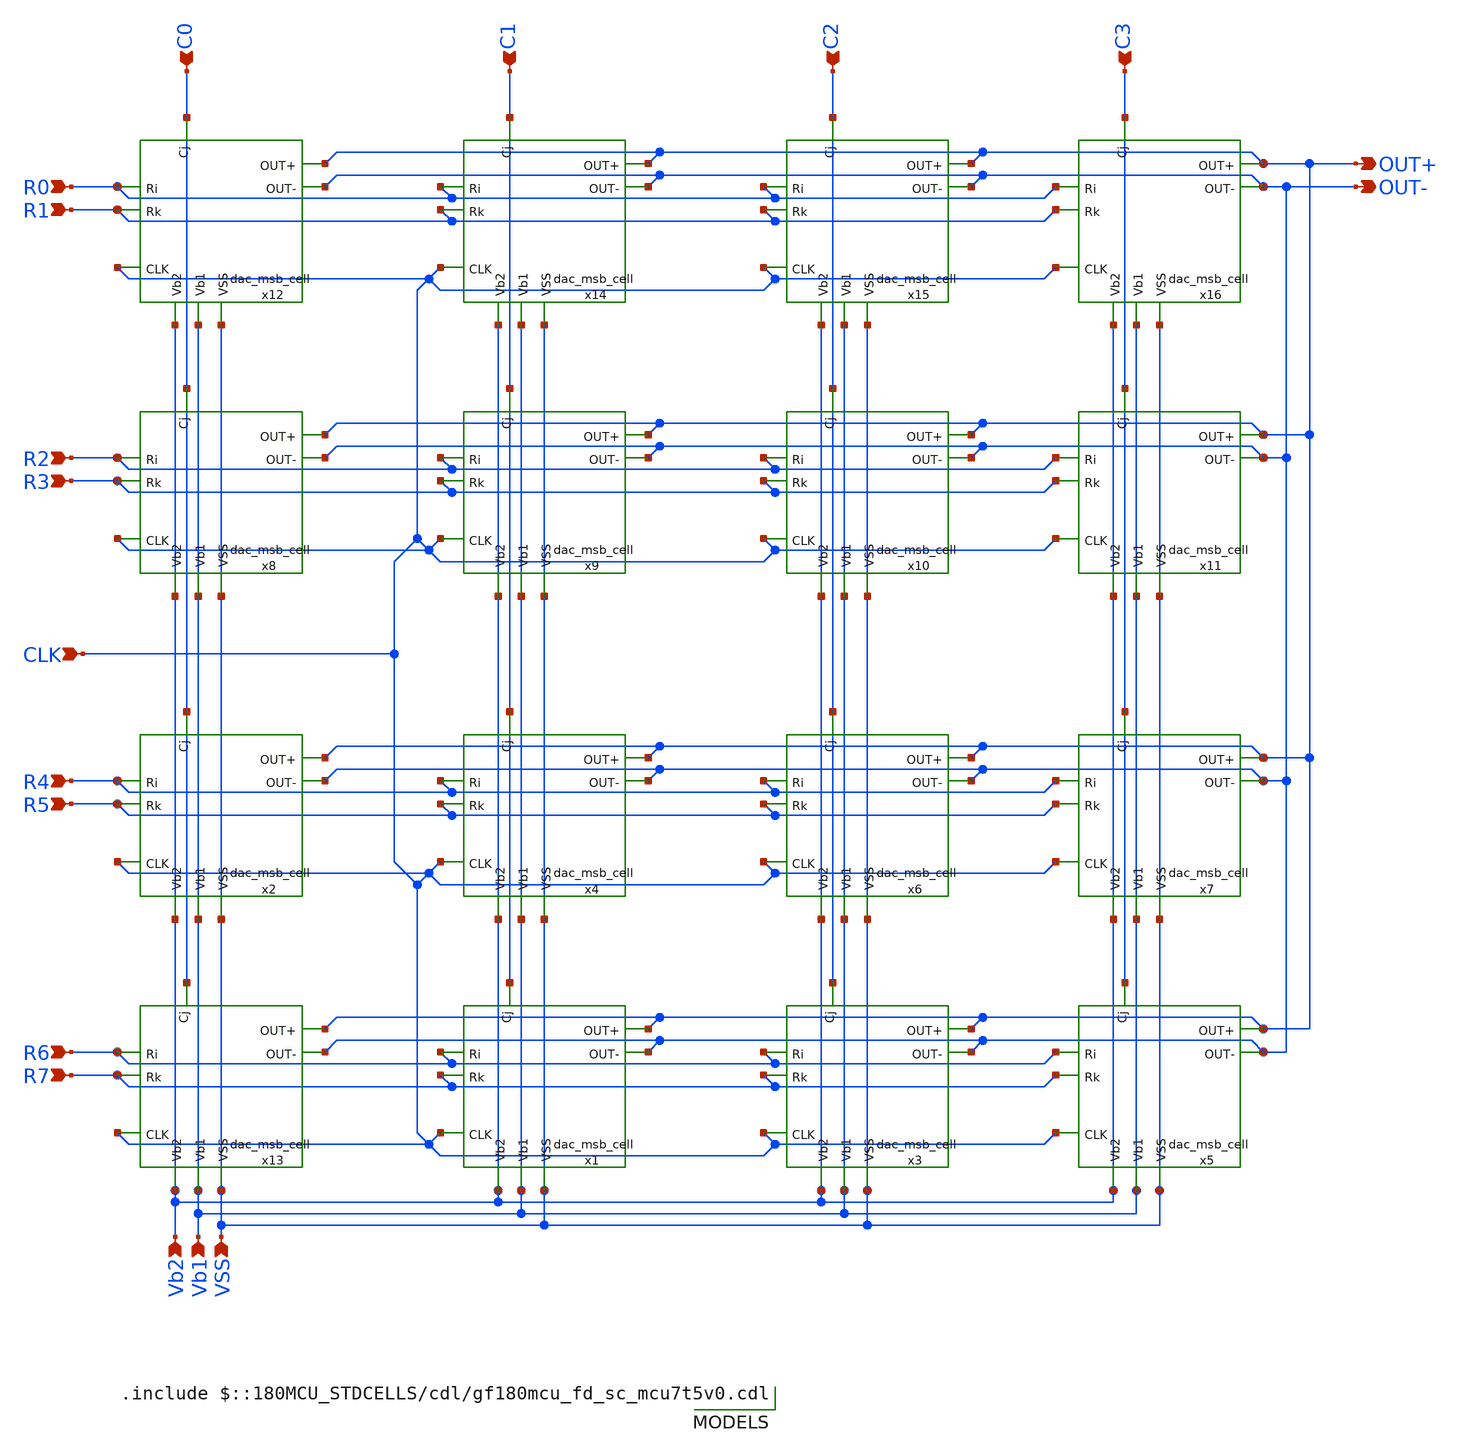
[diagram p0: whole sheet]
** sch_path: DAC/xschem/dac_msb_quarter_matrix.sch
**.subckt dac_msb_quarter_matrix CLK R0 R1 R2 R3 R4 R5 R6 R7 C0 C1 C2 C3 VSS Vb2 Vb1 OUT+ OUT-
*.ipin CLK
*.ipin R0
*.ipin R1
*.ipin R2
*.ipin R3
*.ipin R4
*.ipin R5
*.ipin R6
*.ipin R7
*.ipin C0
*.ipin C1
*.ipin C2
*.ipin C3
*.ipin VSS
*.ipin Vb2
*.ipin Vb1
*.opin OUT+
*.opin OUT-
x13 C0 R6 R7 CLK Vb2 Vb1 VSS OUT+ OUT- DVDD DVSS dac_msb_cell
x1 C1 R6 R7 CLK Vb2 Vb1 VSS OUT+ OUT- DVDD DVSS dac_msb_cell
x3 C2 R6 R7 CLK Vb2 Vb1 VSS OUT+ OUT- DVDD DVSS dac_msb_cell
x5 C3 R6 R7 CLK Vb2 Vb1 VSS OUT+ OUT- DVDD DVSS dac_msb_cell
x2 C0 R4 R5 CLK Vb2 Vb1 VSS OUT+ OUT- DVDD DVSS dac_msb_cell
x4 C1 R4 R5 CLK Vb2 Vb1 VSS OUT+ OUT- DVDD DVSS dac_msb_cell
x6 C2 R4 R5 CLK Vb2 Vb1 VSS OUT+ OUT- DVDD DVSS dac_msb_cell
x7 C3 R4 R5 CLK Vb2 Vb1 VSS OUT+ OUT- DVDD DVSS dac_msb_cell
x8 C0 R2 R3 CLK Vb2 Vb1 VSS OUT+ OUT- DVDD DVSS dac_msb_cell
x9 C1 R2 R3 CLK Vb2 Vb1 VSS OUT+ OUT- DVDD DVSS dac_msb_cell
x10 C2 R2 R3 CLK Vb2 Vb1 VSS OUT+ OUT- DVDD DVSS dac_msb_cell
x11 C3 R2 R3 CLK Vb2 Vb1 VSS OUT+ OUT- DVDD DVSS dac_msb_cell
x12 C0 R0 R1 CLK Vb2 Vb1 VSS OUT+ OUT- DVDD DVSS dac_msb_cell
x14 C1 R0 R1 CLK Vb2 Vb1 VSS OUT+ OUT- DVDD DVSS dac_msb_cell
x15 C2 R0 R1 CLK Vb2 Vb1 VSS OUT+ OUT- DVDD DVSS dac_msb_cell
x16 C3 R0 R1 CLK Vb2 Vb1 VSS OUT+ OUT- DVDD DVSS dac_msb_cell
**** begin user architecture code

.include $::180MCU_STDCELLS/cdl/gf180mcu_fd_sc_mcu7t5v0.cdl

**** end user architecture code
**.ends

* expanding   symbol:  dac_msb_cell.sym # of pins=9
** sym_path: DAC/xschem/dac_msb_cell.sym
** sch_path: DAC/xschem/dac_msb_cell.sch
.subckt dac_msb_cell Cj Ri Rk CLK Vb2 Vb1 VSS OUT+ OUT- DVDD DVSS
*.ipin Cj
*.ipin Rk
*.ipin Ri
*.ipin CLK
*.ipin Vb2
*.ipin Vb1
*.ipin VSS
*.opin OUT+
*.opin OUT-
x2 net4 CLK net1 DVDD DVDD DVSS DVSS gf180mcu_fd_sc_mcu7t5v0__dffq_1
x3 net1 net2 DVDD DVDD DVSS DVSS gf180mcu_fd_sc_mcu7t5v0__inv_1
x6 Cj Ri net3 DVDD DVDD DVSS DVSS gf180mcu_fd_sc_mcu7t5v0__and2_1
x4 net3 Rk net4 DVDD DVDD DVSS DVSS gf180mcu_fd_sc_mcu7t5v0__or2_1
x1 OUT+ OUT- net2 net1 Vb2 Vb1 VSS dac_msb_analog
.ends


* expanding   symbol:  dac_msb_analog.sym # of pins=7
** sym_path: DAC/xschem/dac_msb_analog.sym
** sch_path: DAC/xschem/dac_msb_analog.sch
.subckt dac_msb_analog OUT+ OUT- Q- Q+ Vb2 Vb1 VSS
*.ipin Q-
*.ipin Q+
*.ipin Vb1
*.ipin Vb2
*.opin OUT+
*.opin OUT-
*.ipin VSS
XM26 net1 Vb2 net2 VSS nfet_03v3 L=0.5u W=32u nf=16 ad='int((nf+1)/2) * W/nf * 0.18u' as='int((nf+2)/2) * W/nf * 0.18u'
+ pd='2*int((nf+1)/2) * (W/nf + 0.18u)' ps='2*int((nf+2)/2) * (W/nf + 0.18u)' nrd='0.18u / W' nrs='0.18u / W'
+ sa=0 sb=0 sd=0 m=1
XM27 net2 Vb1 VSS VSS nfet_03v3 L=0.5u W=32u nf=16 ad='int((nf+1)/2) * W/nf * 0.18u' as='int((nf+2)/2) * W/nf * 0.18u'
+ pd='2*int((nf+1)/2) * (W/nf + 0.18u)' ps='2*int((nf+2)/2) * (W/nf + 0.18u)' nrd='0.18u / W' nrs='0.18u / W'
+ sa=0 sb=0 sd=0 m=1
XM30 OUT+ Q+ net1 VSS nfet_03v3 L=0.5u W=16u nf=8 ad='int((nf+1)/2) * W/nf * 0.18u' as='int((nf+2)/2) * W/nf * 0.18u'
+ pd='2*int((nf+1)/2) * (W/nf + 0.18u)' ps='2*int((nf+2)/2) * (W/nf + 0.18u)' nrd='0.18u / W' nrs='0.18u / W'
+ sa=0 sb=0 sd=0 m=1
XM31 OUT- Q- net1 VSS nfet_03v3 L=0.5u W=16u nf=8 ad='int((nf+1)/2) * W/nf * 0.18u' as='int((nf+2)/2) * W/nf * 0.18u'
+ pd='2*int((nf+1)/2) * (W/nf + 0.18u)' ps='2*int((nf+2)/2) * (W/nf + 0.18u)' nrd='0.18u / W' nrs='0.18u / W'
+ sa=0 sb=0 sd=0 m=1
.ends

.end
